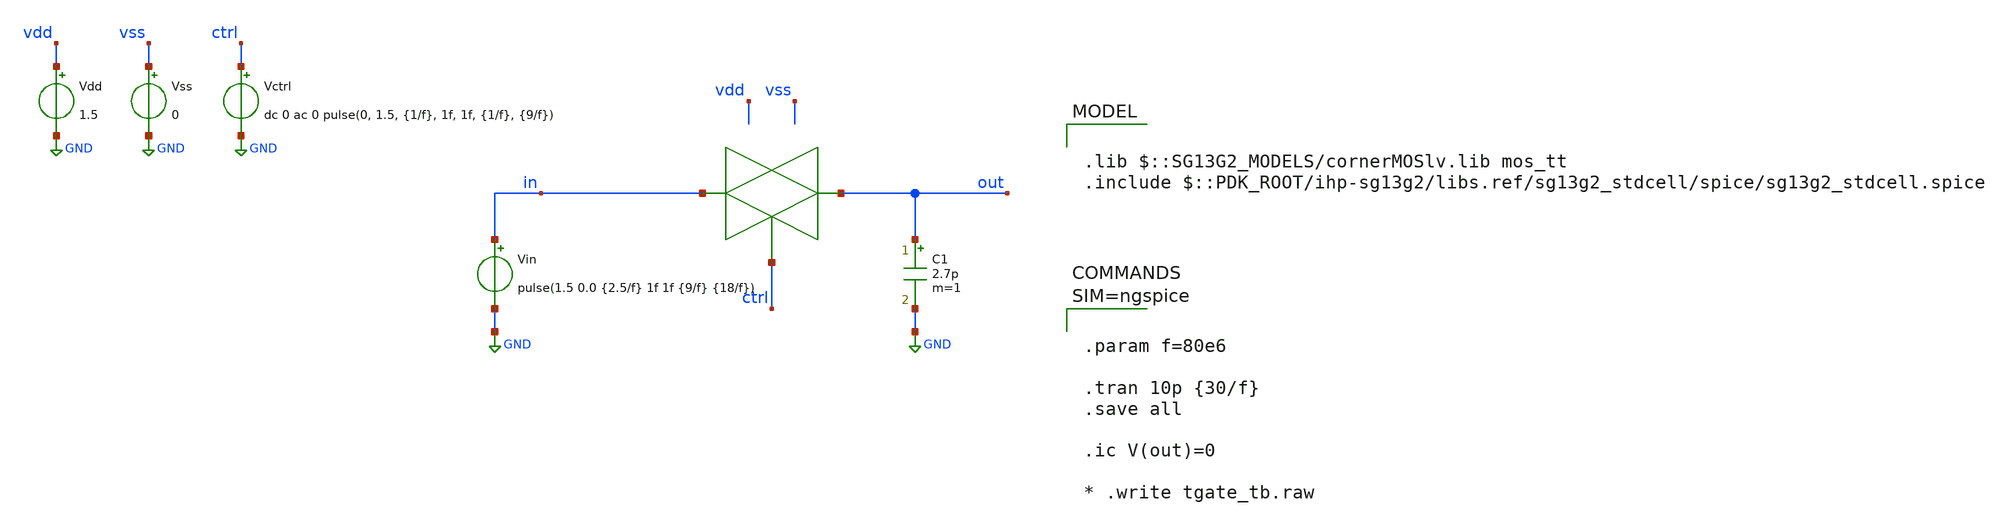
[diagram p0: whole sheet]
** sch_path: designs/tgate_time/tgate_tb.sch
**.subckt tgate_tb
Vdd vdd GND 1.5
Vss vss GND 0
C1 out GND 2.7p m=1
Vin in GND pulse(1.5 0.0 {2.5/f} 1f 1f {9/f} {18/f})
Vctrl ctrl GND dc 0 ac 0 pulse(0, 1.5, {1/f}, 1f, 1f, {1/f}, {9/f})
**** begin user architecture code



.param f=80e6

.tran 10p {30/f}
.save all

.ic V(out)=0

* .write tgate_tb.raw




.lib $::SG13G2_MODELS/cornerMOSlv.lib mos_tt
.include $::PDK_ROOT/ihp-sg13g2/libs.ref/sg13g2_stdcell/spice/sg13g2_stdcell.spice

**** end user architecture code
**.ends
.GLOBAL GND
.end
